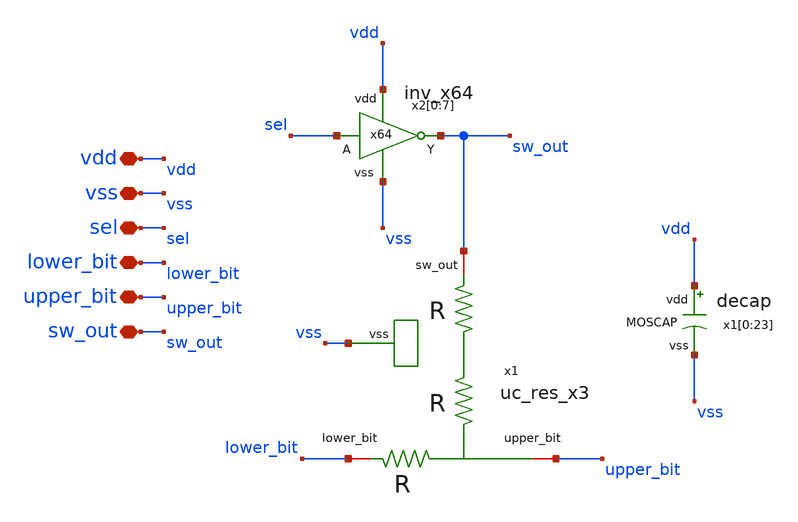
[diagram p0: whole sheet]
** sch_path: xschem/uc_res+sw/uc_res+sw.sch
**.subckt uc_res+sw vdd vss sel lower_bit upper_bit sw_out
*.iopin vdd
*.iopin vss
*.iopin sel
*.iopin lower_bit
*.iopin upper_bit
*.iopin sw_out
x1 sw_out upper_bit lower_bit vss uc_res_x3
x2[0] vdd sw_out sel vss inv_x64
x2[1] vdd sw_out sel vss inv_x64
x2[2] vdd sw_out sel vss inv_x64
x2[3] vdd sw_out sel vss inv_x64
x2[4] vdd sw_out sel vss inv_x64
x2[5] vdd sw_out sel vss inv_x64
x2[6] vdd sw_out sel vss inv_x64
x2[7] vdd sw_out sel vss inv_x64
x1[0] vdd vss decap
x1[1] vdd vss decap
x1[2] vdd vss decap
x1[3] vdd vss decap
x1[4] vdd vss decap
x1[5] vdd vss decap
x1[6] vdd vss decap
x1[7] vdd vss decap
x1[8] vdd vss decap
x1[9] vdd vss decap
x1[10] vdd vss decap
x1[11] vdd vss decap
x1[12] vdd vss decap
x1[13] vdd vss decap
x1[14] vdd vss decap
x1[15] vdd vss decap
x1[16] vdd vss decap
x1[17] vdd vss decap
x1[18] vdd vss decap
x1[19] vdd vss decap
x1[20] vdd vss decap
x1[21] vdd vss decap
x1[22] vdd vss decap
x1[23] vdd vss decap
**.ends

* expanding   symbol:  /foss/designs/dac10b-r2r-sky130/xschem/uc_res_x3/uc_res_x3.sym # of pins=4
** sym_path: xschem/uc_res_x3/uc_res_x3.sym
** sch_path: xschem/uc_res_x3/uc_res_x3.sch
.subckt uc_res_x3 sw_out upper_bit lower_bit vss
*.iopin sw_out
*.iopin upper_bit
*.iopin lower_bit
*.iopin vss
XR1 net1 sw_out vss sky130_fd_pr__res_xhigh_po_1p41 L=14.1 mult=1 m=1
XR2 upper_bit net1 vss sky130_fd_pr__res_xhigh_po_1p41 L=14.1 mult=1 m=1
XR3 lower_bit upper_bit vss sky130_fd_pr__res_xhigh_po_1p41 L=14.1 mult=1 m=1
.ends


* expanding   symbol:  /foss/designs/dac10b-r2r-sky130/xschem/inv_xN/inv_x64.sym # of pins=4
** sym_path: xschem/inv_xN/inv_x64.sym
** sch_path: xschem/inv_xN/inv_x64.sch
.subckt inv_x64 vdd Y A vss
*.ipin A
*.ipin vdd
*.ipin vss
*.opin Y
x_inv[0] vdd Y A vss inv_x1
x_inv[1] vdd Y A vss inv_x1
x_inv[2] vdd Y A vss inv_x1
x_inv[3] vdd Y A vss inv_x1
x_inv[4] vdd Y A vss inv_x1
x_inv[5] vdd Y A vss inv_x1
x_inv[6] vdd Y A vss inv_x1
x_inv[7] vdd Y A vss inv_x1
x_inv[8] vdd Y A vss inv_x1
x_inv[9] vdd Y A vss inv_x1
x_inv[10] vdd Y A vss inv_x1
x_inv[11] vdd Y A vss inv_x1
x_inv[12] vdd Y A vss inv_x1
x_inv[13] vdd Y A vss inv_x1
x_inv[14] vdd Y A vss inv_x1
x_inv[15] vdd Y A vss inv_x1
x_inv[16] vdd Y A vss inv_x1
x_inv[17] vdd Y A vss inv_x1
x_inv[18] vdd Y A vss inv_x1
x_inv[19] vdd Y A vss inv_x1
x_inv[20] vdd Y A vss inv_x1
x_inv[21] vdd Y A vss inv_x1
x_inv[22] vdd Y A vss inv_x1
x_inv[23] vdd Y A vss inv_x1
x_inv[24] vdd Y A vss inv_x1
x_inv[25] vdd Y A vss inv_x1
x_inv[26] vdd Y A vss inv_x1
x_inv[27] vdd Y A vss inv_x1
x_inv[28] vdd Y A vss inv_x1
x_inv[29] vdd Y A vss inv_x1
x_inv[30] vdd Y A vss inv_x1
x_inv[31] vdd Y A vss inv_x1
x_inv[32] vdd Y A vss inv_x1
x_inv[33] vdd Y A vss inv_x1
x_inv[34] vdd Y A vss inv_x1
x_inv[35] vdd Y A vss inv_x1
x_inv[36] vdd Y A vss inv_x1
x_inv[37] vdd Y A vss inv_x1
x_inv[38] vdd Y A vss inv_x1
x_inv[39] vdd Y A vss inv_x1
x_inv[40] vdd Y A vss inv_x1
x_inv[41] vdd Y A vss inv_x1
x_inv[42] vdd Y A vss inv_x1
x_inv[43] vdd Y A vss inv_x1
x_inv[44] vdd Y A vss inv_x1
x_inv[45] vdd Y A vss inv_x1
x_inv[46] vdd Y A vss inv_x1
x_inv[47] vdd Y A vss inv_x1
x_inv[48] vdd Y A vss inv_x1
x_inv[49] vdd Y A vss inv_x1
x_inv[50] vdd Y A vss inv_x1
x_inv[51] vdd Y A vss inv_x1
x_inv[52] vdd Y A vss inv_x1
x_inv[53] vdd Y A vss inv_x1
x_inv[54] vdd Y A vss inv_x1
x_inv[55] vdd Y A vss inv_x1
x_inv[56] vdd Y A vss inv_x1
x_inv[57] vdd Y A vss inv_x1
x_inv[58] vdd Y A vss inv_x1
x_inv[59] vdd Y A vss inv_x1
x_inv[60] vdd Y A vss inv_x1
x_inv[61] vdd Y A vss inv_x1
x_inv[62] vdd Y A vss inv_x1
x_inv[63] vdd Y A vss inv_x1
.ends


* expanding   symbol:  /foss/designs/dac10b-r2r-sky130/xschem/decap/decap.sym # of pins=2
** sym_path: xschem/decap/decap.sym
** sch_path: xschem/decap/decap.sch
.subckt decap vdd vss
*.iopin vdd
*.iopin vss
XM2 vss vdd vss vss sky130_fd_pr__nfet_01v8 L=0.17 W=1 nf=1 ad={int((nf+1)/2) * W/nf * 0.29} as={int((nf+2)/2) * W/nf * 0.29}
+ pd={2*int((nf+1)/2) * (W/nf + 0.29)} ps={2*int((nf+2)/2) * (W/nf + 0.29)} nrd={0.29 / W} nrs={0.29 / W}
+ sa=0 sb=0 sd=0 mult=1 m=1
XM1 vdd vss vdd vdd sky130_fd_pr__pfet_01v8 L=0.17 W=1 nf=1 ad={int((nf+1)/2) * W/nf * 0.29} as={int((nf+2)/2) * W/nf * 0.29}
+ pd={2*int((nf+1)/2) * (W/nf + 0.29)} ps={2*int((nf+2)/2) * (W/nf + 0.29)} nrd={0.29 / W} nrs={0.29 / W}
+ sa=0 sb=0 sd=0 mult=1 m=1
.ends

.end
